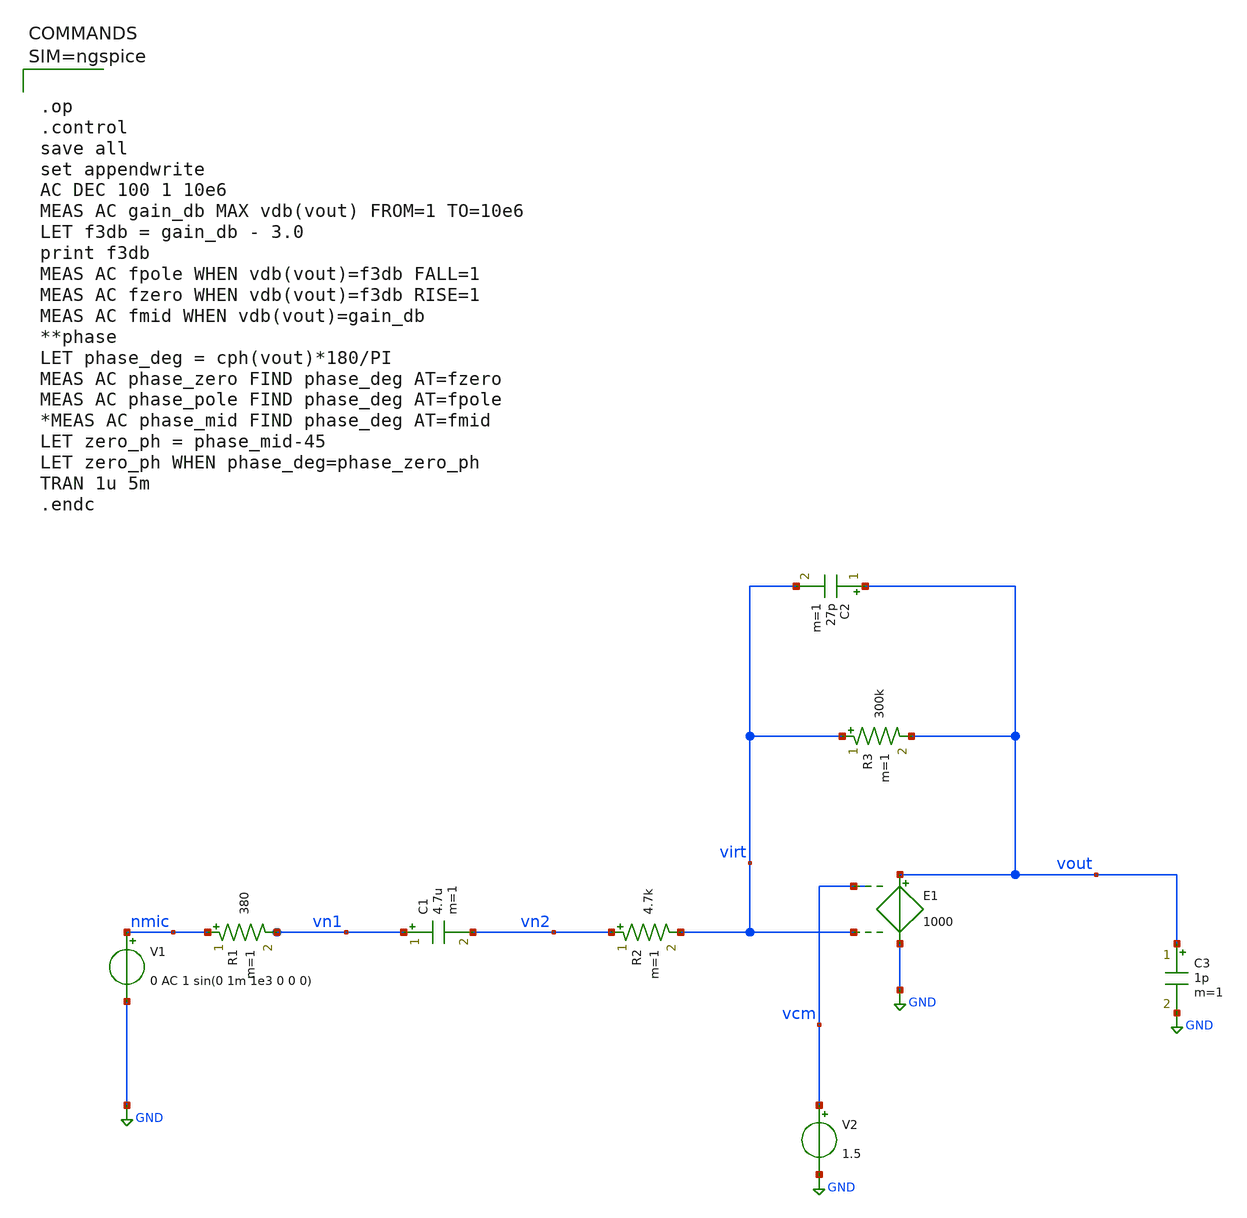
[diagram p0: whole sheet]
** sch_path: xschem/mictest1.sch
**.subckt mictest1
V1 nmic GND 0 AC 1 sin(0 1m 1e3 0 0 0)
R1 nmic vn1 380 m=1
C1 vn1 vn2 4.7u m=1
R2 vn2 virt 4.7k m=1
E1 vout GND vcm virt 1000
R3 virt vout 300k m=1
C2 vout virt 27p m=1
V2 vcm GND 1.5
C3 vout GND 1p m=1
**** begin user architecture code



.op
.control
save all
set appendwrite
AC DEC 100 1 10e6
MEAS AC gain_db MAX vdb(vout) FROM=1 TO=10e6
LET f3db = gain_db - 3.0
print f3db
MEAS AC fpole WHEN vdb(vout)=f3db FALL=1
MEAS AC fzero WHEN vdb(vout)=f3db RISE=1
MEAS AC fmid WHEN vdb(vout)=gain_db
**phase
LET phase_deg = cph(vout)*180/PI
MEAS AC phase_zero FIND phase_deg AT=fzero
MEAS AC phase_pole FIND phase_deg AT=fpole
*MEAS AC phase_mid FIND phase_deg AT=fmid
LET zero_ph = phase_mid-45
LET zero_ph WHEN phase_deg=phase_zero_ph
TRAN 1u 5m
.endc





**** end user architecture code
**.ends
.GLOBAL GND
.end
